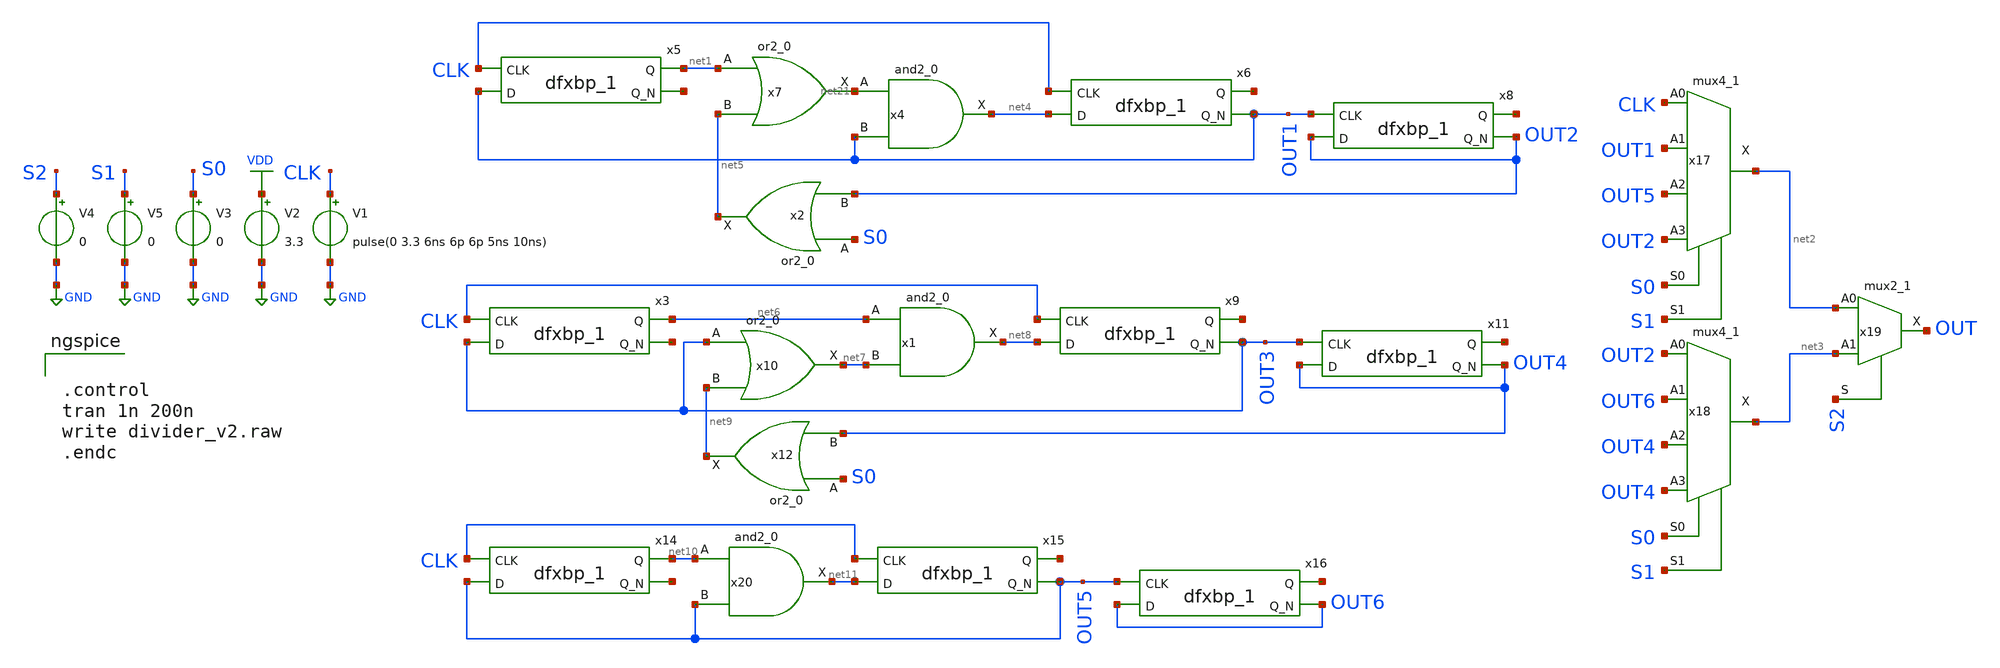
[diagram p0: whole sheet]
** sch_path: Frequency Divider/divider_v2.sch
**.subckt divider_v2
V1 CLK GND pulse(0 3.3 6ns 6p 6p 5ns 10ns)
V2 VDD GND 3.3
x5 CLK OUT1 GND GND VDD VDD net1 net12 sky130_fd_sc_hd__dfxbp_1
x6 CLK net4 GND GND VDD VDD net13 OUT1 sky130_fd_sc_hd__dfxbp_1
x8 OUT1 OUT2 GND GND VDD VDD net14 OUT2 sky130_fd_sc_hd__dfxbp_1
x3 CLK OUT3 GND GND VDD VDD net6 net15 sky130_fd_sc_hd__dfxbp_1
x9 CLK net8 GND GND VDD VDD net16 OUT3 sky130_fd_sc_hd__dfxbp_1
x11 OUT3 OUT4 GND GND VDD VDD net17 OUT4 sky130_fd_sc_hd__dfxbp_1
x14 CLK OUT5 GND GND VDD VDD net10 net18 sky130_fd_sc_hd__dfxbp_1
x15 CLK net11 GND GND VDD VDD net19 OUT5 sky130_fd_sc_hd__dfxbp_1
x16 OUT5 OUT6 GND GND VDD VDD net20 OUT6 sky130_fd_sc_hd__dfxbp_1
x17 CLK OUT1 OUT5 OUT2 S0 S1 GND GND VDD VDD net2 sky130_fd_sc_hd__mux4_1
x18 OUT2 OUT6 OUT4 OUT4 S0 S1 GND GND VDD VDD net3 sky130_fd_sc_hd__mux4_1
x19 net2 net3 S2 GND GND VDD VDD OUT sky130_fd_sc_hd__mux2_1
V3 S0 GND 0
V4 S2 GND 0
V5 S1 GND 0
x20 net10 OUT5 GND GND VDD VDD net11 sky130_fd_sc_hd__and2_0
x7 net1 net5 GND GND VDD VDD net21 sky130_fd_sc_hd__or2_0
x4 net21 OUT1 GND GND VDD VDD net4 sky130_fd_sc_hd__and2_0
x2 S0 OUT2 GND GND VDD VDD net5 sky130_fd_sc_hd__or2_0
x10 OUT3 net9 GND GND VDD VDD net7 sky130_fd_sc_hd__or2_0
x12 S0 OUT4 GND GND VDD VDD net9 sky130_fd_sc_hd__or2_0
x1 net6 net7 GND GND VDD VDD net8 sky130_fd_sc_hd__and2_0
**** begin user architecture code


.control
tran 1n 200n
write divider_v2.raw
.endc




.include /home/xuan/pdk/sky130A/libs.ref/sky130_fd_sc_hd/spice/sky130_fd_sc_hd.spice





** opencircuitdesign pdks install
.lib $::SKYWATER_MODELS/sky130.lib.spice tt


**** end user architecture code
**.ends
.GLOBAL GND
.GLOBAL VDD
.end
